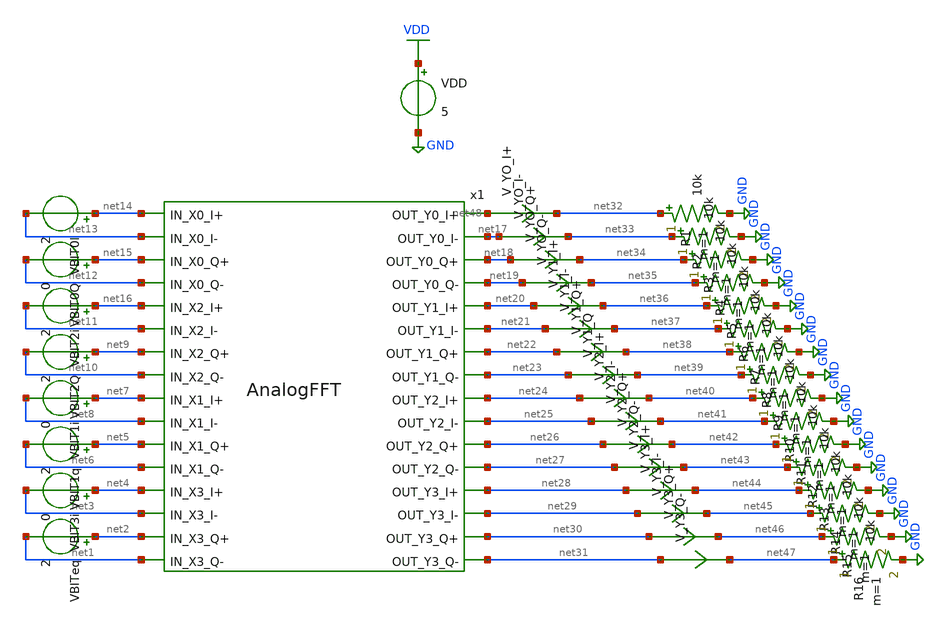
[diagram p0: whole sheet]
** sch_path: xschem/FinalProject/AnalogFFTTB.sch
**.subckt AnalogFFTTB
x1 net14 net48 net13 net17 net15 net18 net12 net19 net16 net20 net11 net21 net9 net22 net10 net23
+ net7 net24 net8 net25 net5 net26 net6 net27 net4 net28 net3 net29 net2 net30 net1 net31 AnalogFFT
VDD VDD GND 5
VBIT0I net14 net13 2
VBIT0Q net15 net12 0
VBIT2i net16 net11 2
VBIT2Q net9 net10 2
VBIT1i net7 net8 0
VBIT1q net5 net6 2
VBIT3i net4 net3 0
VBITeq net2 net1 2
V_YO_I+ net48 net32 0
.save i(v_yo_i+)
V_YO_I- net17 net33 0
.save i(v_yo_i-)
V_YO_Q+ net18 net34 0
.save i(v_yo_q+)
V_YO_Q- net19 net35 0
.save i(v_yo_q-)
V_Y1_I+ net20 net36 0
.save i(v_y1_i+)
V_Y1_I- net21 net37 0
.save i(v_y1_i-)
V_Y1_Q+ net22 net38 0
.save i(v_y1_q+)
V_Y1_Q net23 net39 0
.save i(v_y1_q)
V_Y2_I+ net24 net40 0
.save i(v_y2_i+)
V_Y2_I- net25 net41 0
.save i(v_y2_i-)
V_Y2_Q+ net26 net42 0
.save i(v_y2_q+)
V_Y2_Q- net27 net43 0
.save i(v_y2_q-)
V_Y3_I+ net28 net44 0
.save i(v_y3_i+)
V_Y3_I- net29 net45 0
.save i(v_y3_i-)
V_Y3_Q+ net30 net46 0
.save i(v_y3_q+)
V_Y3_Q- net31 net47 0
.save i(v_y3_q-)
R1 net32 GND 10k m=1
R2 net33 GND 10k m=1
R3 net34 GND 10k m=1
R4 net35 GND 10k m=1
R5 net36 GND 10k m=1
R6 net37 GND 10k m=1
R7 net38 GND 10k m=1
R8 net39 GND 10k m=1
R9 net40 GND 10k m=1
R10 net41 GND 10k m=1
R11 net42 GND 10k m=1
R12 net43 GND 10k m=1
R13 net44 GND 10k m=1
R14 net45 GND 10k m=1
R15 net46 GND 10k m=1
R16 net47 GND 10k m=1
**** begin user architecture code

** opencircuitdesign pdks install
.lib $::SKYWATER_MODELS/sky130.lib.spice tt



* this option enables mos model bin
* selection based on W/NF instead of W
.include ~/Project/mag/AnalogFFT.spice
.control
op
*dc VDD 1 4 0.01
print all
save all
.endc


**** end user architecture code
**.ends
.GLOBAL VDD
.GLOBAL GND
.end
